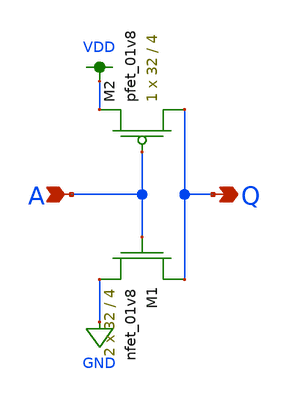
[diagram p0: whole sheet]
** sch_path: schemas/inv.sch
**.subckt inv A Q
*.ipin A
*.opin Q
XM1 Q A GND GND sky130_fd_pr__nfet_01v8 L=4 W=32 nf=1 ad='int((nf+1)/2) * W/nf * 0.29' as='int((nf+2)/2) * W/nf * 0.29'
+ pd='2*int((nf+1)/2) * (W/nf + 0.29)' ps='2*int((nf+2)/2) * (W/nf + 0.29)' nrd='0.29 / W' nrs='0.29 / W'
+ sa=0 sb=0 sd=0 mult=2 m=2
XM2 Q A VDD VDD sky130_fd_pr__pfet_01v8 L=4 W=32 nf=1 ad='int((nf+1)/2) * W/nf * 0.29' as='int((nf+2)/2) * W/nf * 0.29'
+ pd='2*int((nf+1)/2) * (W/nf + 0.29)' ps='2*int((nf+2)/2) * (W/nf + 0.29)' nrd='0.29 / W' nrs='0.29 / W'
+ sa=0 sb=0 sd=0 mult=1 m=1
**.ends
.GLOBAL VDD
.GLOBAL GND
.end
